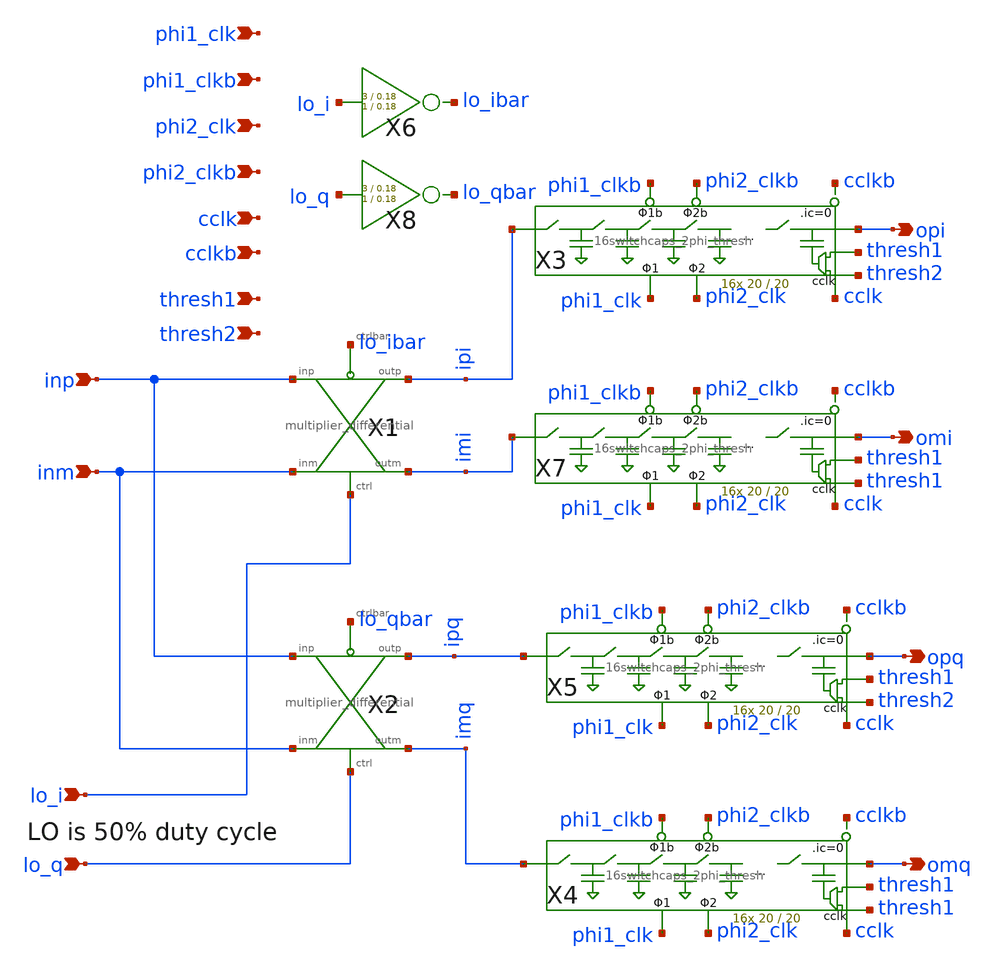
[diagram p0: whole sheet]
** sch_path: xschem/wavelet_channel/wavelet_iq.sch
**.subckt wavelet_iq inp inm phi1_clk phi2_clk lo_q lo_i opi omi phi1_clkb phi2_clkb cclk cclkb
*+ thresh1 thresh2 opq omq
*.ipin inp
*.ipin inm
*.ipin phi1_clk
*.ipin phi2_clk
*.ipin lo_q
*.ipin lo_i
*.opin opi
*.opin omi
*.ipin phi1_clkb
*.ipin phi2_clkb
*.ipin cclk
*.ipin cclkb
*.ipin thresh1
*.ipin thresh2
*.opin opq
*.opin omq
X1 inp ipi inm lo_i imi lo_ibar multiplier_differential
X2 inp ipq inm lo_q imq lo_qbar multiplier_differential
X7 imi omi phi1_clk phi1_clkb phi2_clk phi2_clkb cclk thresh1 thresh1 cclkb 16switchcaps_2phi_thresh
+ W=20 L=20
X3 ipi opi phi1_clk phi1_clkb phi2_clk phi2_clkb cclk thresh1 thresh2 cclkb 16switchcaps_2phi_thresh
+ W=20 L=20
X4 imq omq phi1_clk phi1_clkb phi2_clk phi2_clkb cclk thresh1 thresh1 cclkb 16switchcaps_2phi_thresh
+ W=20 L=20
X5 ipq opq phi1_clk phi1_clkb phi2_clk phi2_clkb cclk thresh1 thresh2 cclkb 16switchcaps_2phi_thresh
+ W=20 L=20
X6 lo_i lo_ibar inv Wpmos=3 Lpmos=0.18 Wnmos=1 Lnmos=0.18
X8 lo_q lo_qbar inv Wpmos=3 Lpmos=0.18 Wnmos=1 Lnmos=0.18
**.ends
.end
